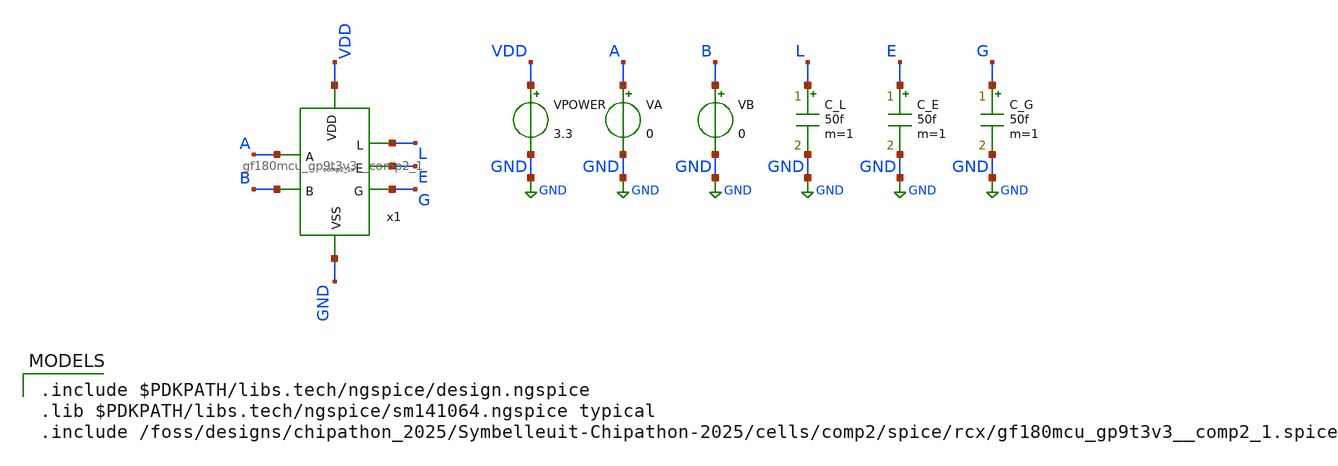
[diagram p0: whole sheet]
** sch_path: cells/comp2/cace/templates/comp2_tb_dc.sch
**.subckt comp2_tb_dc
x1 VDD L A E G B GND gf180mcu_gp9t3v3__comp2_1
VPOWER VDD GND 3.3
VA A GND 0
VB B GND 0
C_L L GND 50f m=1
C_E E GND 50f m=1
C_G G GND 50f m=1
**** begin user architecture code

.include $PDKPATH/libs.tech/ngspice/design.ngspice
.lib $PDKPATH/libs.tech/ngspice/sm141064.ngspice typical
.include /foss/designs/chipathon_2025/Symbelleuit-Chipathon-2025/cells/comp2/spice/rcx/gf180mcu_gp9t3v3__comp2_1.spice


* CACE DC Transfer Switching Threshold Simulation
.control
  dc VA 0 3.3 0.02
  meas dc vm_G_sweepA WHEN v(G) = 1.65 CROSS=1
  print vm_G_sweepA
  echo $&vm_G_sweepA > comp2_tb_dc_0.data
.endc
.GLOBAL GND


**** end user architecture code
**.ends
.GLOBAL GND
.end
